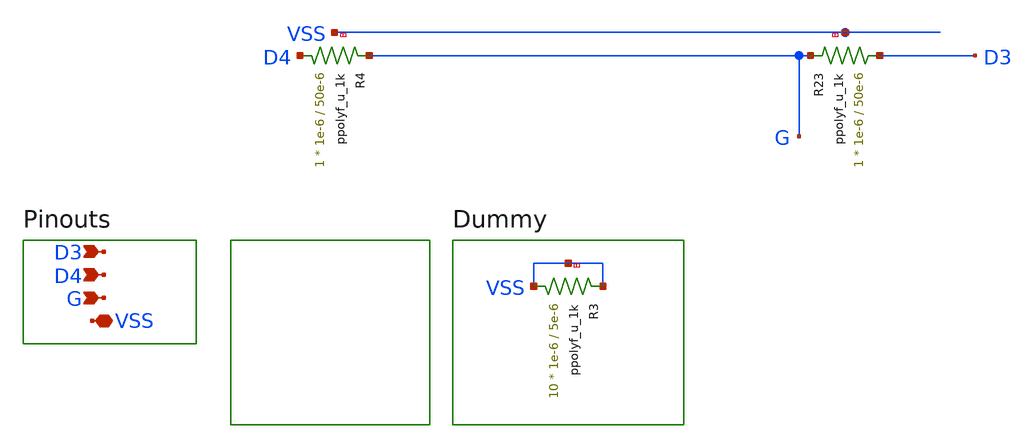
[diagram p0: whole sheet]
** sch_path: designs/libs/core_ota/differential_load_res/differential_load_res.sch
**.subckt differential_load_res VSS D3 D4 G
*.iopin VSS
*.ipin D3
*.ipin D4
*.ipin G
XR3 VSS VSS VSS ppolyf_u_1k r_width=1e-6 r_length=5e-6 m=10
XR4 D4 G VSS ppolyf_u_1k r_width=1e-6 r_length=50e-6 m=1
XR23 D3 G VSS ppolyf_u_1k r_width=1e-6 r_length=50e-6 m=1
**.ends
.end
